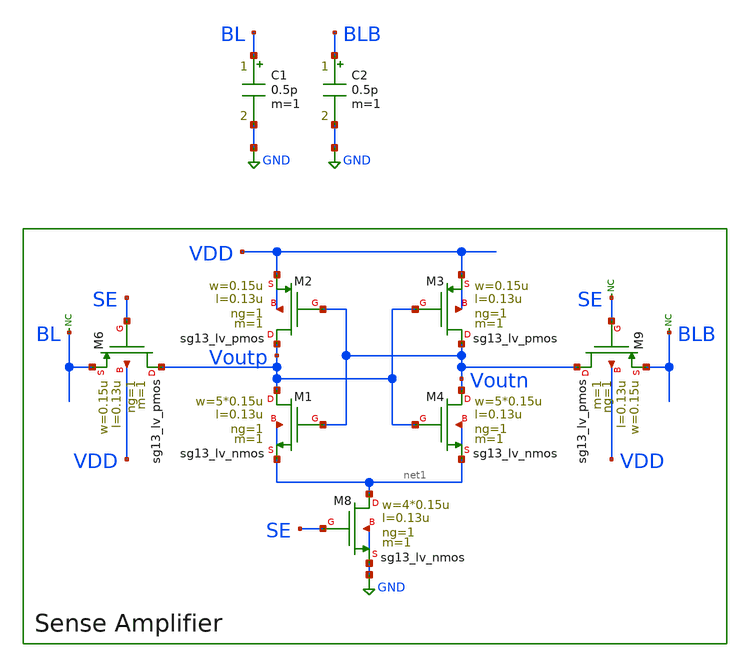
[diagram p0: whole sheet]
** sch_path: xschem/offset_voltage_tester/offset-voltage-tester.sch
**.subckt offset-voltage-tester
XM8 net1 SE GND GND sg13_lv_nmos w=4*0.15u l=0.13u ng=1 m=1 mm_ok=1
XM1 Voutp Voutn net1 net1 sg13_lv_nmos w=5*0.15u l=0.13u ng=1 m=1 mm_ok=1
XM3 Voutn Voutp VDD VDD sg13_lv_pmos w=0.15u l=0.13u ng=1 m=1 mm_ok=1
XM2 Voutp Voutn VDD VDD sg13_lv_pmos w=0.15u l=0.13u ng=1 m=1 mm_ok=1
XM4 Voutn Voutp net1 net1 sg13_lv_nmos w=5*0.15u l=0.13u ng=1 m=1 mm_ok=1
XM6 Voutp SE BL VDD sg13_lv_pmos w=0.15u l=0.13u ng=1 m=1 mm_ok=1
XM9 Voutn SE BLB VDD sg13_lv_pmos w=0.15u l=0.13u ng=1 m=1 mm_ok=1
* noconn SE
* noconn BLB
* noconn BL
C1 BL GND 0.5p m=1
C2 BLB GND 0.5p m=1
**** begin user architecture code



.lib cornerMOSlv.lib mos_tt_mismatch

.param mm_ok=1
.param mc_ok=1
.param temp=27

.param VDD=1.2
.param VCM=1.175
.param VIND_INIT=0

.param TPER=10n
.param TSE_DLY=4n
.param TSE_W=3n
.param TR=100p
.param TF=100p
.param TEVAL=6.5n

VDD_S VDD 0 {VDD}

* SE Pulse:
* 0V -> VDD @ TSE_DLY
* Stays high for TSE_W
* Repeats every TPER
VSE SE 0 PULSE(0 {VDD} {TSE_DLY} {TR} {TF} {TSE_W} {TPER})

VVIND VIND_CTRL 0 {VIND_INIT}

B_BLDRV BLDRV 0 V = {VCM + v(VIND_CTRL) / 2}
B_BLBDRV BLBDRV 0 V = {VCM - v(VIND_CTRL) / 2}

RBL BLDRV BL 50
RBLB BLBDRV BLB 50

.control

set noaskquit
set numdgt=10
set wr_singlescale
set wr_vecnames

let mc_runs = 500

let vin_min = -0.05
let vin_max = 0.05
let vind_range = vin_max - vin_min
let nbit = 10
let voutd_th = 0

let tstep = 20p
let tper = 10n
let teval = 6.5n

let max_cycles = 4 * nbit + 4
let tstop = max_cycles * tper

setplot new
set scratch = $curplot

let run = 0
dowhile run < mc_runs
    source /foss/designs/sram-sense-amp/xschem/offset_voltage_tester/offset_voltage_tester.sp

    let run = run + 1
end

rusage time

.endc



**** end user architecture code
**.ends
.GLOBAL GND
.end
